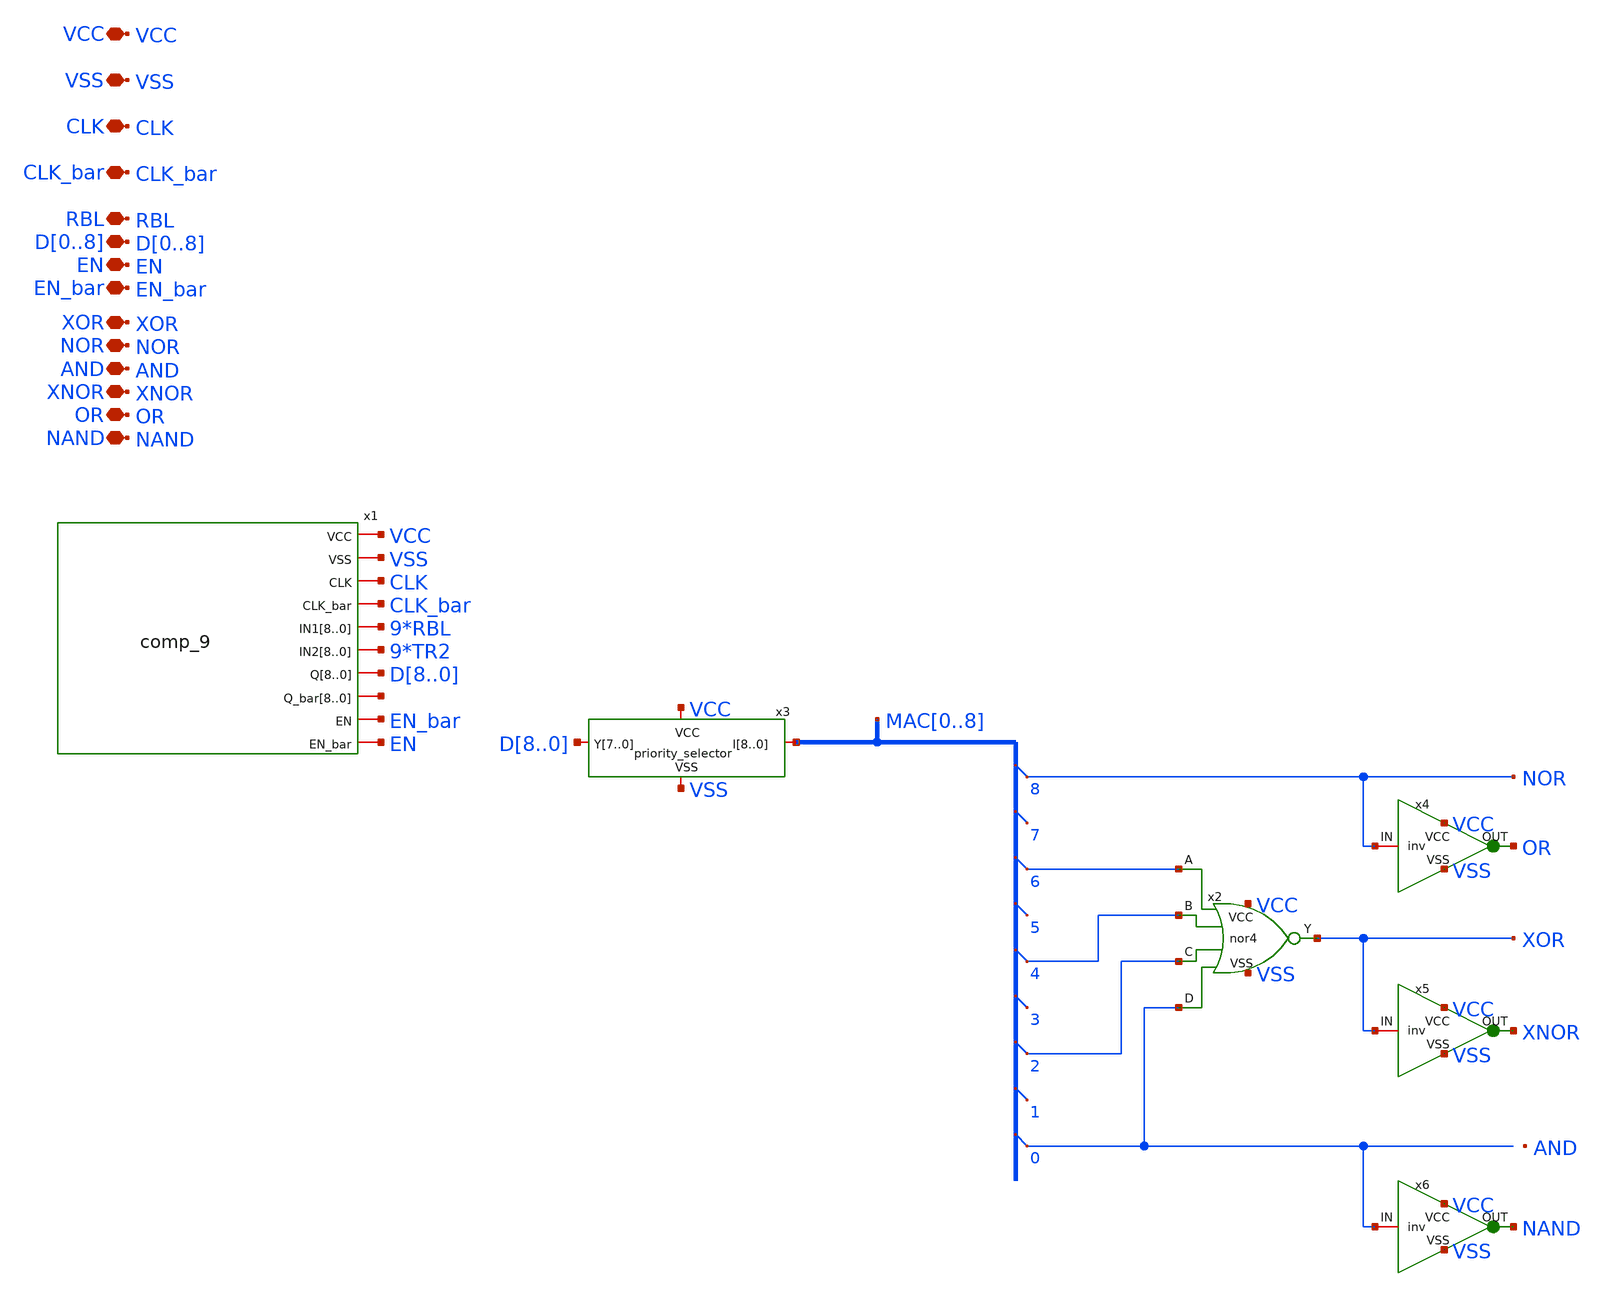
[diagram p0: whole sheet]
** sch_path: voltage_comp/temp.sch
**.subckt temp VSS VCC CLK CLK_bar EN EN_bar XOR NOR AND D0,D1,D2,D3,D4,D5,D6,D7,D8 XNOR OR NAND RBL
*.iopin VSS
*.iopin VCC
*.iopin CLK
*.iopin CLK_bar
*.iopin EN
*.iopin EN_bar
*.iopin XOR
*.iopin NOR
*.iopin AND
*.iopin D0,D1,D2,D3,D4,D5,D6,D7,D8
*.iopin XNOR
*.iopin OR
*.iopin NAND
*.iopin RBL
x1 VCC VSS CLK CLK_bar RBL RBL RBL RBL RBL RBL RBL RBL RBL TR2 TR2 TR2 TR2 TR2 TR2 TR2 TR2 TR2 D8 D7
+ D6 D5 D4 D3 D2 D1 D0 net1[8] net1[7] net1[6] net1[5] net1[4] net1[3] net1[2] net1[1] net1[0] EN_bar EN
+ comp_9
* tap: MAC[0..8] --> MAC0
* tap: MAC[0..8] --> MAC1
* tap: MAC[0..8] --> MAC2
* tap: MAC[0..8] --> MAC3
* tap: MAC[0..8] --> MAC4
* tap: MAC[0..8] --> MAC5
* tap: MAC[0..8] --> MAC6
* tap: MAC[0..8] --> MAC7
* tap: MAC[0..8] --> MAC8
x2 VCC XOR MAC6 MAC2 MAC4 MAC0 VSS nor4
x3 VCC VSS MAC0 MAC1 MAC2 MAC3 MAC4 MAC5 MAC6 MAC7 MAC8 D8 D7 D6 D5 D4 D3 D2 D1 priority_selector
x4 VCC MAC8 OR VSS inv
x5 VCC XOR XNOR VSS inv
x6 VCC MAC0 NAND VSS inv
**.ends
.end
